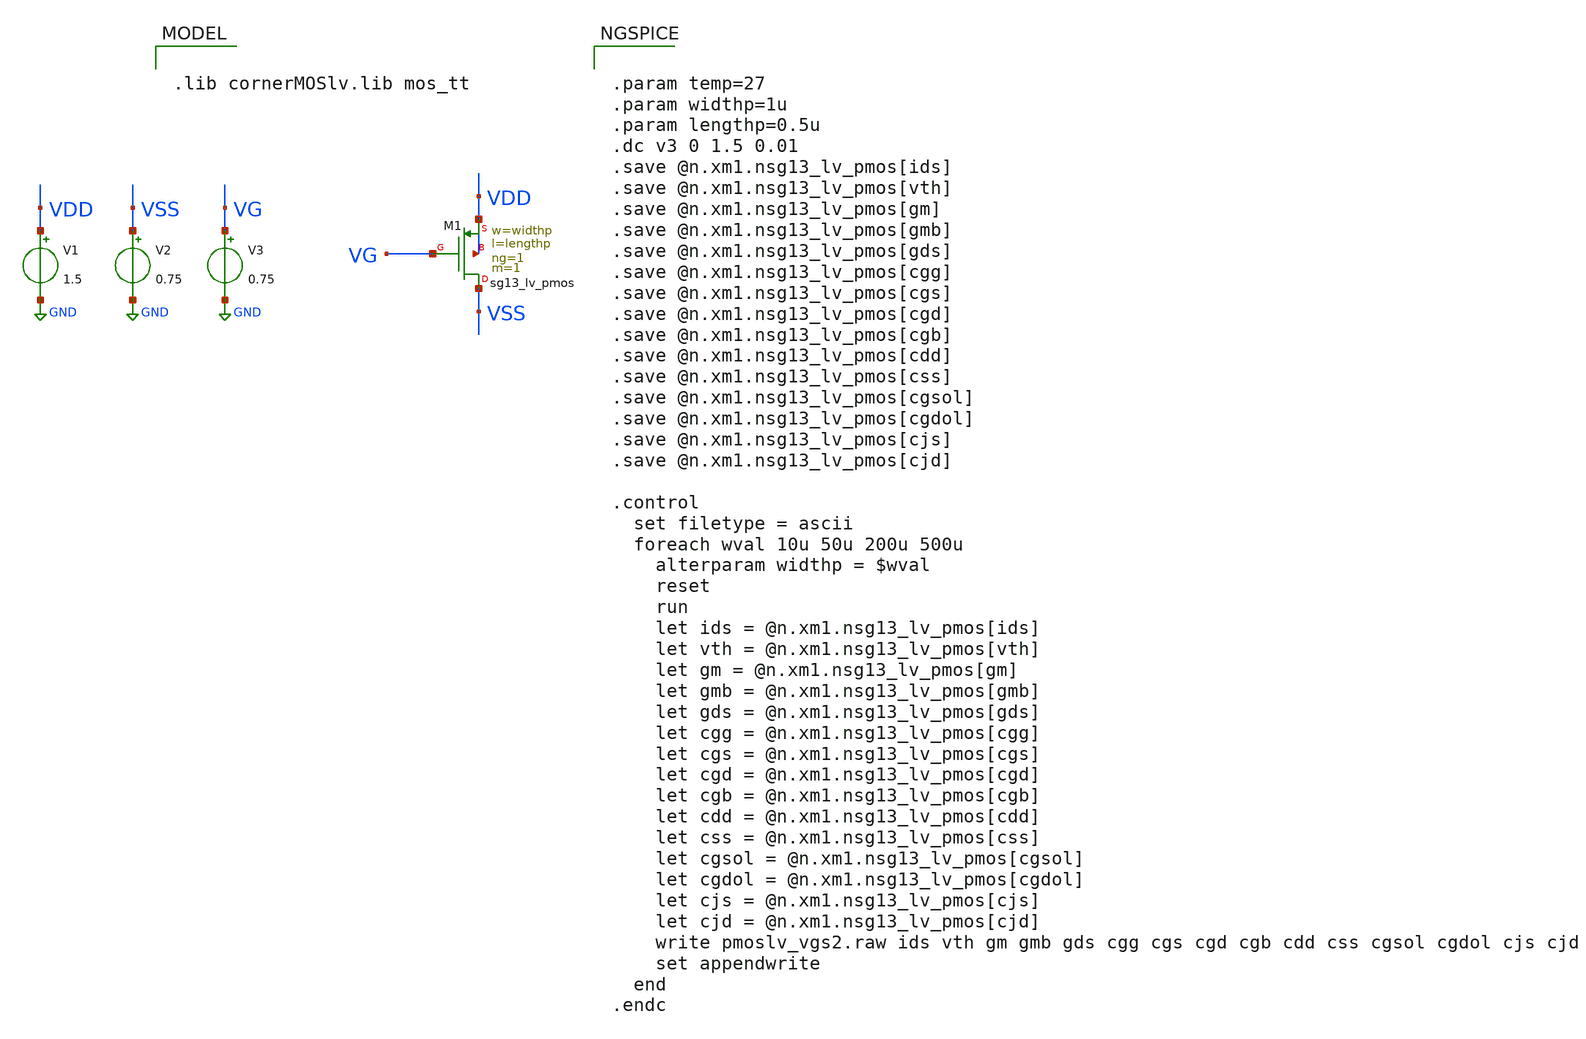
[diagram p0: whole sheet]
** sch_path: analog/tb/tb_pmos_lv_vgs.sch
**.subckt tb_pmos_lv_vgs
V1 VDD GND 1.5
V2 VSS GND 0.75
V3 VG GND 0.75
XM1 VSS VG VDD VDD sg13_lv_pmos w=widthp l=lengthp ng=1 m=1 mm_ok=1
**** begin user architecture code


.param temp=27
.param widthp=1u
.param lengthp=0.5u
.dc v3 0 1.5 0.01
.save @n.xm1.nsg13_lv_pmos[ids]
.save @n.xm1.nsg13_lv_pmos[vth]
.save @n.xm1.nsg13_lv_pmos[gm]
.save @n.xm1.nsg13_lv_pmos[gmb]
.save @n.xm1.nsg13_lv_pmos[gds]
.save @n.xm1.nsg13_lv_pmos[cgg]
.save @n.xm1.nsg13_lv_pmos[cgs]
.save @n.xm1.nsg13_lv_pmos[cgd]
.save @n.xm1.nsg13_lv_pmos[cgb]
.save @n.xm1.nsg13_lv_pmos[cdd]
.save @n.xm1.nsg13_lv_pmos[css]
.save @n.xm1.nsg13_lv_pmos[cgsol]
.save @n.xm1.nsg13_lv_pmos[cgdol]
.save @n.xm1.nsg13_lv_pmos[cjs]
.save @n.xm1.nsg13_lv_pmos[cjd]

.control
  set filetype = ascii
  foreach wval 10u 50u 200u 500u
    alterparam widthp = $wval
    reset
    run
    let ids = @n.xm1.nsg13_lv_pmos[ids]
    let vth = @n.xm1.nsg13_lv_pmos[vth]
    let gm = @n.xm1.nsg13_lv_pmos[gm]
    let gmb = @n.xm1.nsg13_lv_pmos[gmb]
    let gds = @n.xm1.nsg13_lv_pmos[gds]
    let cgg = @n.xm1.nsg13_lv_pmos[cgg]
    let cgs = @n.xm1.nsg13_lv_pmos[cgs]
    let cgd = @n.xm1.nsg13_lv_pmos[cgd]
    let cgb = @n.xm1.nsg13_lv_pmos[cgb]
    let cdd = @n.xm1.nsg13_lv_pmos[cdd]
    let css = @n.xm1.nsg13_lv_pmos[css]
    let cgsol = @n.xm1.nsg13_lv_pmos[cgsol]
    let cgdol = @n.xm1.nsg13_lv_pmos[cgdol]
    let cjs = @n.xm1.nsg13_lv_pmos[cjs]
    let cjd = @n.xm1.nsg13_lv_pmos[cjd]
    write pmoslv_vgs2.raw ids vth gm gmb gds cgg cgs cgd cgb cdd css cgsol cgdol cjs cjd
    set appendwrite
  end
.endc





.lib cornerMOSlv.lib mos_tt


**** end user architecture code
**.ends
.GLOBAL GND
.end
